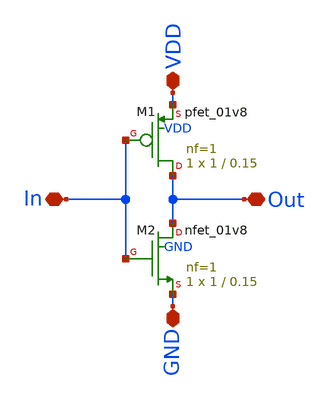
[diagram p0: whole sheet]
** sch_path: VCO_circuit/inverter.sch
**.subckt inverter Out In VDD GND
*.iopin Out
*.iopin In
*.iopin VDD
*.iopin GND
XM1 Out In VDD VDD sky130_fd_pr__pfet_01v8 L=0.15 W=1 nf=1 ad='int((nf+1)/2) * W/nf * 0.29' as='int((nf+2)/2) * W/nf * 0.29'
+ pd='2*int((nf+1)/2) * (W/nf + 0.29)' ps='2*int((nf+2)/2) * (W/nf + 0.29)' nrd='0.29 / W' nrs='0.29 / W'
+ sa=0 sb=0 sd=0 mult=1 m=1
XM2 Out In GND GND sky130_fd_pr__nfet_01v8 L=0.15 W=1 nf=1 ad='int((nf+1)/2) * W/nf * 0.29' as='int((nf+2)/2) * W/nf * 0.29'
+ pd='2*int((nf+1)/2) * (W/nf + 0.29)' ps='2*int((nf+2)/2) * (W/nf + 0.29)' nrd='0.29 / W' nrs='0.29 / W'
+ sa=0 sb=0 sd=0 mult=1 m=1
**.ends
.end
